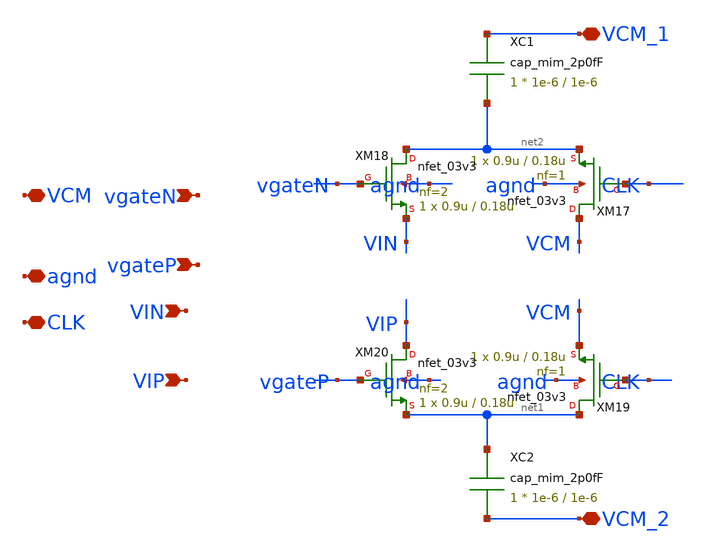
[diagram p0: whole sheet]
** sch_path: mpw18h1/cisar-gen/xschem/TBD/sample_unit.sch
**.subckt sample_unit VCM vgateN VCM_1 vgateP VCM_2 agnd VIN VIP CLK
*.iopin VCM
*.ipin vgateN
*.iopin VCM_1
*.ipin vgateP
*.iopin VCM_2
*.iopin agnd
*.ipin VIN
*.ipin VIP
*.iopin CLK
XM17 VCM CLK net2 agnd nfet_03v3 L=0.18u W=0.9u nf=1 ad='int((nf+1)/2) * W/nf * 0.18u' as='int((nf+2)/2) * W/nf * 0.18u'
+ pd='2*int((nf+1)/2) * (W/nf + 0.18u)' ps='2*int((nf+2)/2) * (W/nf + 0.18u)' nrd='0.18u / W' nrs='0.18u / W'
+ sa=0 sb=0 sd=0 m=1 par=1
XM18 net2 vgateN VIN agnd nfet_03v3 L=0.18u W=0.9u nf=2 ad='int((nf+1)/2) * W/nf * 0.18u' as='int((nf+2)/2) * W/nf * 0.18u'
+ pd='2*int((nf+1)/2) * (W/nf + 0.18u)' ps='2*int((nf+2)/2) * (W/nf + 0.18u)' nrd='0.18u / W' nrs='0.18u / W'
+ sa=0 sb=0 sd=0 m=1 par=1
XM19 net1 CLK VCM agnd nfet_03v3 L=0.18u W=0.9u nf=1 ad='int((nf+1)/2) * W/nf * 0.18u' as='int((nf+2)/2) * W/nf * 0.18u'
+ pd='2*int((nf+1)/2) * (W/nf + 0.18u)' ps='2*int((nf+2)/2) * (W/nf + 0.18u)' nrd='0.18u / W' nrs='0.18u / W'
+ sa=0 sb=0 sd=0 m=1 par=1
XM20 VIP vgateP net1 agnd nfet_03v3 L=0.18u W=0.9u nf=2 ad='int((nf+1)/2) * W/nf * 0.18u' as='int((nf+2)/2) * W/nf * 0.18u'
+ pd='2*int((nf+1)/2) * (W/nf + 0.18u)' ps='2*int((nf+2)/2) * (W/nf + 0.18u)' nrd='0.18u / W' nrs='0.18u / W'
+ sa=0 sb=0 sd=0 m=1 par=1
XC1 VCM_1 net2 cap_mim_2p0fF c_width=1e-6 c_length=1e-6 m=1
XC2 net1 VCM_2 cap_mim_2p0fF c_width=1e-6 c_length=1e-6 m=1
**.ends
.end
